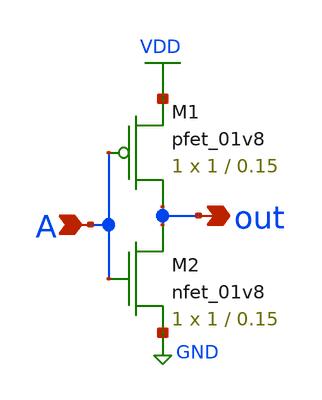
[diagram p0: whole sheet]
** sch_path: MP1/INV_mp1.sch
**.subckt INV_mp1 A out
*.ipin A
*.opin out
XM1 out A VDD VDD sky130_fd_pr__pfet_01v8 L=0.15 W=1 nf=1 ad='int((nf+1)/2) * W/nf * 0.29' as='int((nf+2)/2) * W/nf * 0.29'
+ pd='2*int((nf+1)/2) * (W/nf + 0.29)' ps='2*int((nf+2)/2) * (W/nf + 0.29)' nrd='0.29 / W' nrs='0.29 / W'
+ sa=0 sb=0 sd=0 mult=1 m=1
XM2 out A GND GND sky130_fd_pr__nfet_01v8 L=0.15 W=1 nf=1 ad='int((nf+1)/2) * W/nf * 0.29' as='int((nf+2)/2) * W/nf * 0.29'
+ pd='2*int((nf+1)/2) * (W/nf + 0.29)' ps='2*int((nf+2)/2) * (W/nf + 0.29)' nrd='0.29 / W' nrs='0.29 / W'
+ sa=0 sb=0 sd=0 mult=1 m=1
**.ends
.GLOBAL GND
.GLOBAL VDD
.end
